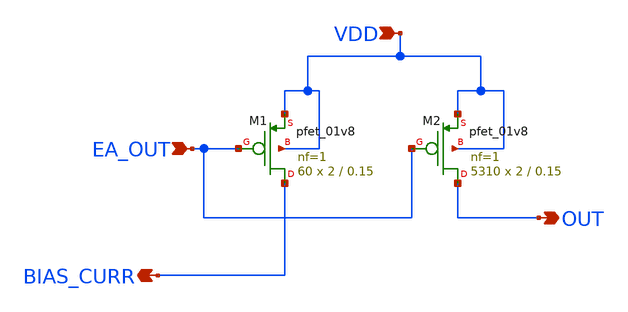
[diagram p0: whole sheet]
** sch_path: xschem/power_transistor.sch
**.subckt power_transistor VDD EA_OUT OUT BIAS_CURR
*.ipin VDD
*.ipin EA_OUT
*.opin OUT
*.opin BIAS_CURR
XM1 BIAS_CURR EA_OUT VDD VDD sky130_fd_pr__pfet_01v8 L=0.15 W=2 nf=1 ad='int((nf+1)/2) * W/nf * 0.29'
+ as='int((nf+2)/2) * W/nf * 0.29' pd='2*int((nf+1)/2) * (W/nf + 0.29)' ps='2*int((nf+2)/2) * (W/nf + 0.29)'
+ nrd='0.29 / W' nrs='0.29 / W' sa=0 sb=0 sd=0 mult=60 m=60
XM2 OUT EA_OUT VDD VDD sky130_fd_pr__pfet_01v8 L=0.15 W=2 nf=1 ad='int((nf+1)/2) * W/nf * 0.29' as='int((nf+2)/2) * W/nf * 0.29'
+ pd='2*int((nf+1)/2) * (W/nf + 0.29)' ps='2*int((nf+2)/2) * (W/nf + 0.29)' nrd='0.29 / W' nrs='0.29 / W'
+ sa=0 sb=0 sd=0 mult=5310 m=5310
**.ends
.end
